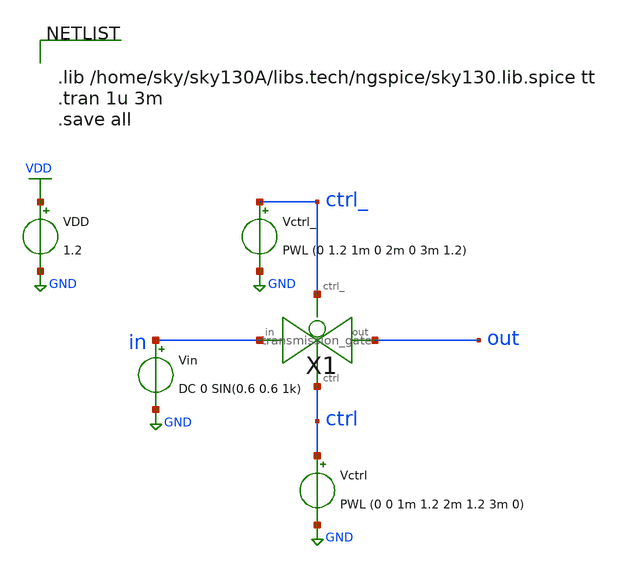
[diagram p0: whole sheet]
** sch_path: xschem/transmission_gate/transmission_gate_tb.sch
**.subckt transmission_gate_tb
X1 in out ctrl_ ctrl transmission_gate
Vin in GND DC 0 SIN(0.6 0.6 1k)
VDD VDD GND 1.2
Vctrl ctrl GND PWL (0 0 1m 1.2 2m 1.2 3m 0)
Vctrl_ ctrl_ GND PWL (0 1.2 1m 0 2m 0 3m 1.2)
**** begin user architecture code


.lib /home/sky/sky130A/libs.tech/ngspice/sky130.lib.spice tt
.tran 1u 3m
.save all


**** end user architecture code
**.ends

* expanding   symbol:  transmission_gate.sym # of pins=4
** sym_path: xschem/transmission_gate/transmission_gate.sym
** sch_path: xschem/transmission_gate/transmission_gate.sch
.subckt transmission_gate in out ctrl_ ctrl
*.iopin in
*.iopin out
*.ipin ctrl_
*.ipin ctrl
XM1 in ctrl out GND sky130_fd_pr__nfet_01v8 L=0.18 W=1 nf=1 ad='int((nf+1)/2) * W/nf * 0.29' as='int((nf+2)/2) * W/nf * 0.29'
+ pd='2*int((nf+1)/2) * (W/nf + 0.29)' ps='2*int((nf+2)/2) * (W/nf + 0.29)' nrd='0.29 / W' nrs='0.29 / W'
+ sa=0 sb=0 sd=0 mult=1 m=1
XM2 out ctrl_ in VDD sky130_fd_pr__pfet_01v8 L=0.18 W=1 nf=1 ad='int((nf+1)/2) * W/nf * 0.29' as='int((nf+2)/2) * W/nf * 0.29'
+ pd='2*int((nf+1)/2) * (W/nf + 0.29)' ps='2*int((nf+2)/2) * (W/nf + 0.29)' nrd='0.29 / W' nrs='0.29 / W'
+ sa=0 sb=0 sd=0 mult=1 m=1
.ends

.GLOBAL VDD
.GLOBAL GND
.end
